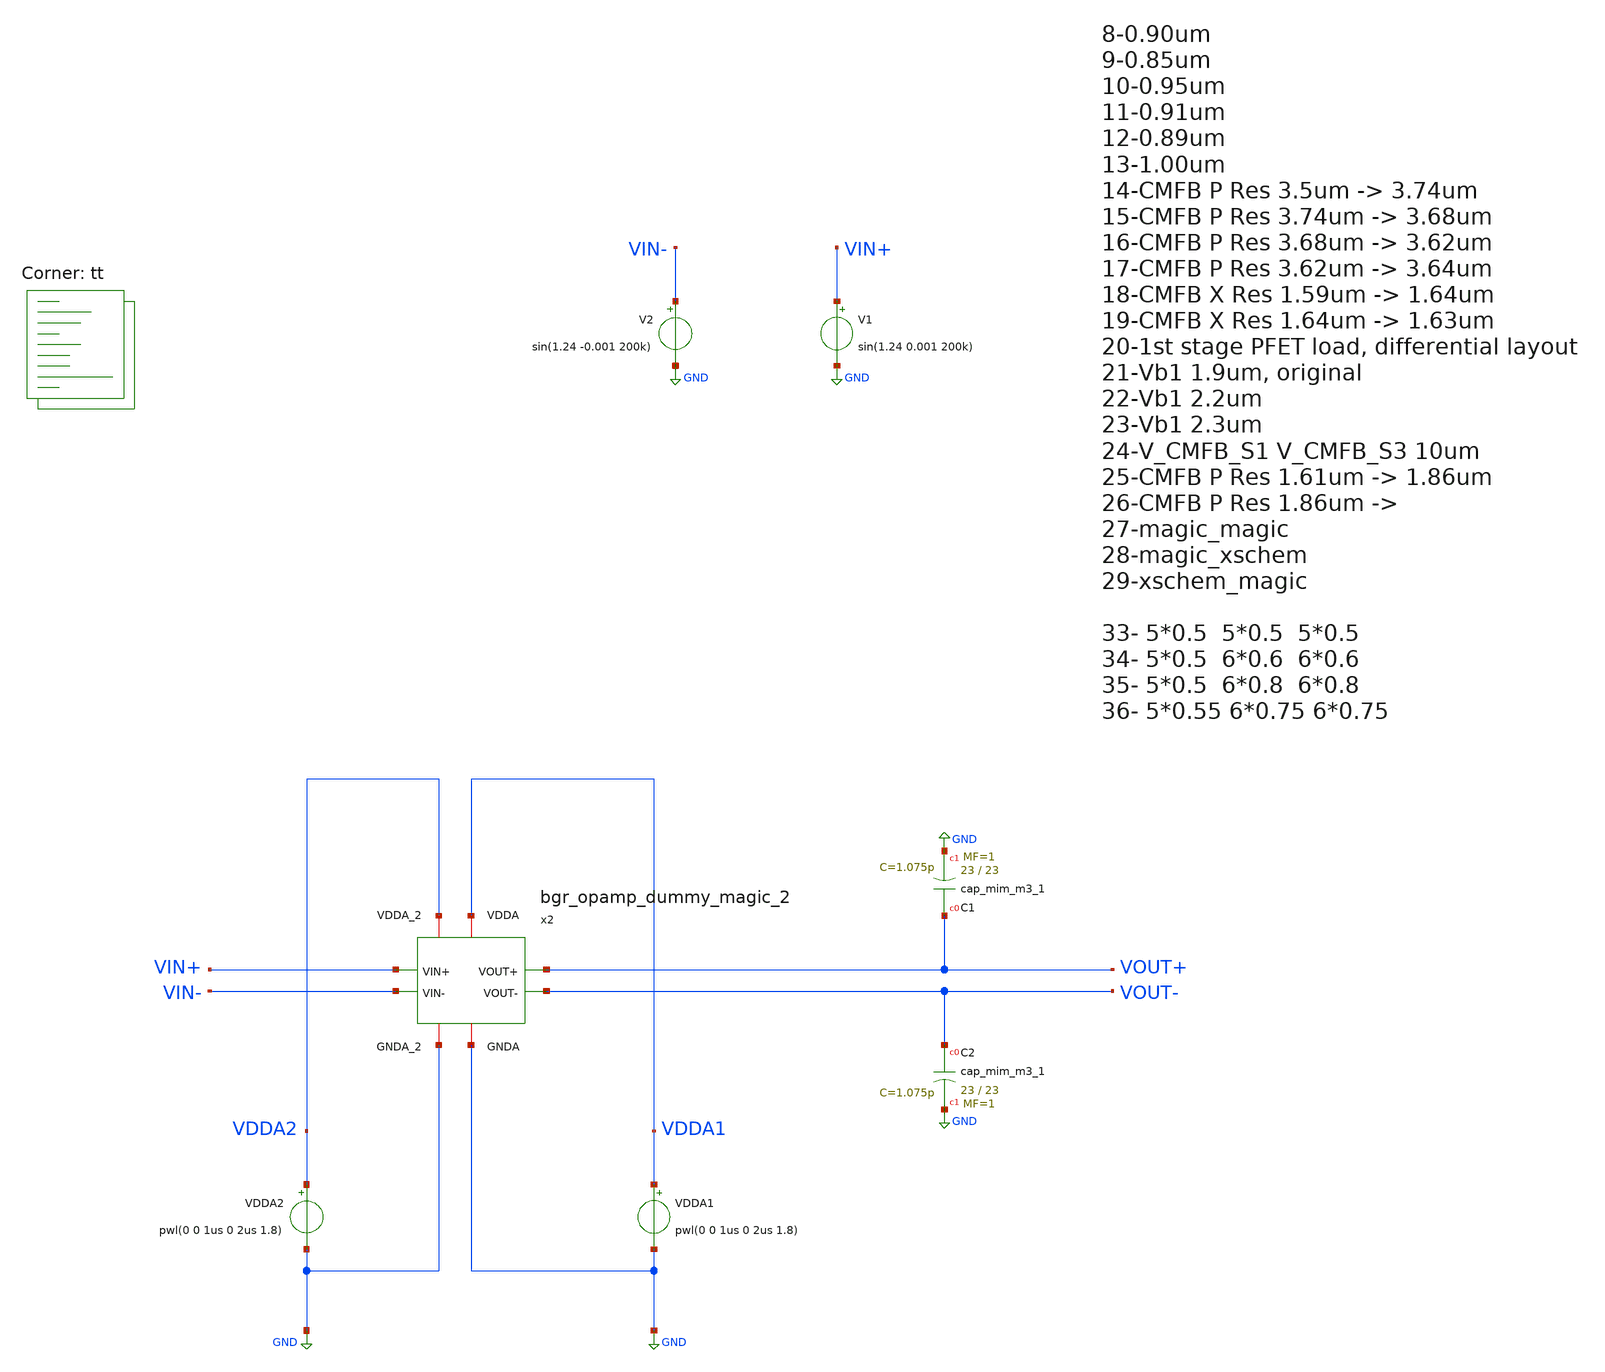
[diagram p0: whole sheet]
** sch_path: projects/opamp/xschem_ngspice/tb_bgr_opamp_dummy_magic_2.sch
**.subckt tb_bgr_opamp_dummy_magic_2
VDDA1 VDDA1 GND pwl(0 0 1us 0 2us 1.8)
V2 VIN- GND sin(1.24 -0.001 200k)
V1 VIN+ GND sin(1.24 0.001 200k)
XC1 VOUT+ GND sky130_fd_pr__cap_mim_m3_1 W=23 L=23 MF=1 m=1
XC2 VOUT- GND sky130_fd_pr__cap_mim_m3_1 W=23 L=23 MF=1 m=1
x2 VDDA1 GND VOUT+ VOUT- VIN+ VIN- VDDA2 GND bgr_opamp_dummy_magic_2
VDDA2 VDDA2 GND pwl(0 0 1us 0 2us 1.8)
**** begin user architecture code
.lib $::SKYWATER_MODELS/sky130.lib.spice tt




* .include /foss/designs/my_design/projects/opamp/xschem_ngspice/bgr_opamp_dummy_magic.spice
.include /foss/designs/my_design/projects/opamp/xschem_ngspice/bgr_opamp_dummy_magic_2.spice
* .include /foss/designs/my_design/projects/opamp/xschem_ngspice/two_stage_opamp_dummy_magic.spice
* .include /foss/designs/my_design/projects/opamp/xschem_ngspice/ref_volt_cur_gen_dummy_magic.spice


.option method=gear
.option wnflag=1
.option savecurrents

.save v(vout+) v(vout-) v(vin+) v(vin-) v(x2.two_stage_opamp_dummy_magic_0.v_cmfb_s1.t0) v(x2.two_stage_opamp_dummy_magic_0.v_cmfb_s2.t0) v(x2.two_stage_opamp_dummy_magic_0.v_cmfb_s3.t0) v(x2.two_stage_opamp_dummy_magic_0.v_cmfb_s4.t0) v(x2.two_stage_opamp_dummy_magic_0.x.t0) v(x2.two_stage_opamp_dummy_magic_0.y.t0) v(x2.two_stage_opamp_dummy_magic_0.v_tot.t0) v(x2.two_stage_opamp_dummy_magic_0.v_err_amp_ref.t0) v(x2.two_stage_opamp_dummy_magic_0.vb1.n0) v(x2.bgr_0.vb1_cur_bias) v(x2.two_stage_opamp_dummy_magic_0.v_source.n0)



* .ic v(v_top) = 1.8

.control

  * let runs=3
  * let run=1

  * dowhile run <= runs
    * save v(vout+) v(vout-) v(vin+) v(vin-) v(v_err_amp_ref) v(x2.x) v(x2.y) v(x2.vb1) v(x2.vb2)
+ v(x2.vb3) v(x2.v_tot)
    save all
    remzerovec
    set appendwrite
    * dc temp -40 120 10 VDD 0 4.0 0.2
    * dc VDD 0 2.0 0.02 temp -40 120 40
    * dc V5 0 0.01 0.0001
    tran 2n 16u
    * tran 10n 150u
    * tran 1p 3n
    * tran 0.1ns 30us
    * ac dec 40 1 10T
    * write tb_bgr_opamp_dummy_magic.raw
    write tb_bgr_opamp_dummy_magic_2.raw
    * write tb_bgr_opamp_dummy_magic_3.raw
    * write tb_bgr_opamp_dummy_magic_4.raw
    * write tb_bgr_opamp_dummy_magic_5.raw
    * write tb_bgr_opamp_dummy_magic_6.raw
    * write tb_bgr_opamp_dummy_magic_7.raw
    * write tb_bgr_opamp_dummy_magic_mc.raw
    * write tb_bgr_opamp_dummy_magic_tt_mm.raw
    * write tb_bgr_opamp_dummy_magic_AC.raw
    * reset
    * let run = run + 1
  * end
.endc




**** end user architecture code
**.ends
.GLOBAL GND
.end
